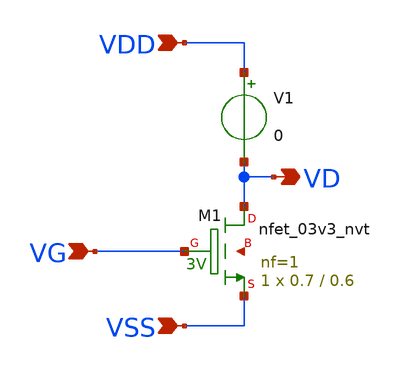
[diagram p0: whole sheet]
** sch_path: design/THESIS_EXP_RO_INVERTER_SKY130A/TB_FET.sch
**.subckt TB_FET VDD VSS VD VG
*.ipin VDD
*.ipin VSS
*.opin VD
*.ipin VG
V1 VDD VD 0
.save i(v1)
XM1 VD VG VSS net1 sky130_fd_pr__nfet_03v3_nvt L=0.6 W=0.7 nf=1 ad='int((nf+1)/2) * W/nf * 0.29' as='int((nf+2)/2) * W/nf * 0.29'
+ pd='2*int((nf+1)/2) * (W/nf + 0.29)' ps='2*int((nf+2)/2) * (W/nf + 0.29)' nrd='0.29 / W' nrs='0.29 / W'
+ sa=0 sb=0 sd=0 mult=1 m=1
**.ends
.end
